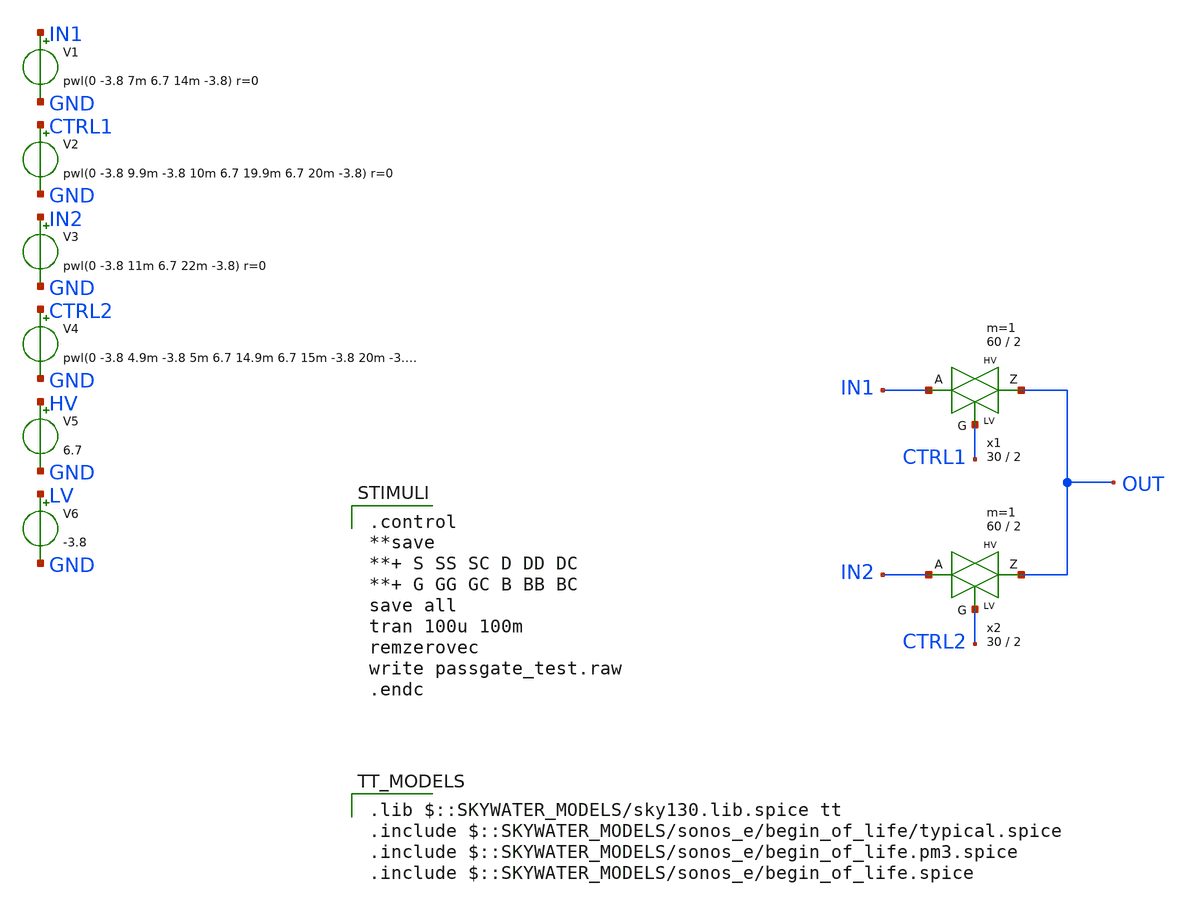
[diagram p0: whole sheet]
** sch_path: passgate_test.sch
* passgate_hv.sch:
* Copyright 2021 Stefan Frederik Schippers
* Licensed under the Apache License, Version 2.0 (the "License");
**.subckt passgate_test
x1 OUT IN1 CTRL1 HV LV passgate_hv W_N=30 L_N=2 W_P=60 L_P=2 m=1
x2 OUT IN2 CTRL2 HV LV passgate_hv W_N=30 L_N=2 W_P=60 L_P=2 m=1
V1 IN1 GND pwl(0 -3.8 7m 6.7 14m -3.8) r=0
V2 CTRL1 GND pwl(0 -3.8 9.9m -3.8 10m 6.7 19.9m 6.7 20m -3.8) r=0
V3 IN2 GND pwl(0 -3.8 11m 6.7 22m -3.8) r=0
V4 CTRL2 GND pwl(0 -3.8 4.9m -3.8 5m 6.7 14.9m 6.7 15m -3.8 20m -3.8) r=0
V5 HV GND 6.7
V6 LV GND -3.8
**** begin user architecture code

.control
**save
**+ S SS SC D DD DC
**+ G GG GC B BB BC
save all
tran 100u 100m
remzerovec
write passgate_test.raw
.endc

 .lib $::SKYWATER_MODELS/sky130.lib.spice tt
.include $::SKYWATER_MODELS/sonos_e/begin_of_life/typical.spice
.include $::SKYWATER_MODELS/sonos_e/begin_of_life.pm3.spice
.include $::SKYWATER_MODELS/sonos_e/begin_of_life.spice
**** end user architecture code
**.ends

* expanding   symbol:  passgate_hv.sym # of pins=3
** sym_path: passgate_hv.sym
** sch_path: passgate_hv.sch
.subckt passgate_hv Z A G VCCBPIN VSSBPIN  W_N=30 L_N=2 W_P=60 L_P=2
*.iopin A
*.iopin Z
*.ipin G
XM2 A net1 Z VCCBPIN sky130_fd_pr__pfet_20v0 L=L_P W=W_P m=1
XM1 A G Z VSSBPIN sky130_fd_pr__nfet_20v0 L=L_N W=W_N m=1
XM3 net1 G VSSBPIN VSSBPIN sky130_fd_pr__nfet_20v0 L=L_N W=W_N m=1
XM4 net1 G VCCBPIN VCCBPIN sky130_fd_pr__pfet_20v0 L=L_P W=W_P m=1
.ends

.end
